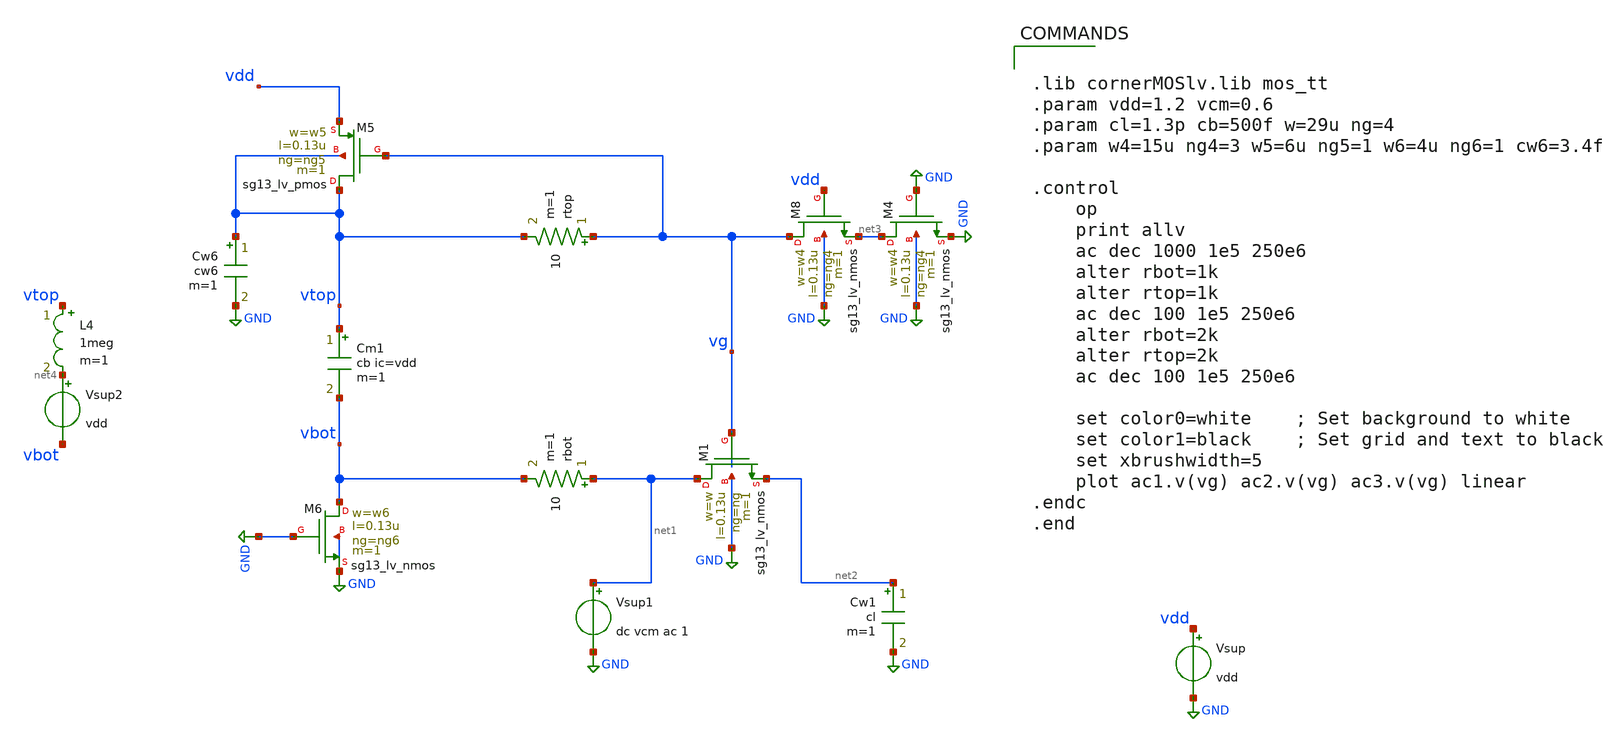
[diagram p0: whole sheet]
** sch_path: xschem/tb_boot3_ac.sch
**.subckt tb_boot3_ac
Vsup vdd GND vdd
Cm1 vtop vbot cb ic=vdd m=1
XM1 net1 vg net2 GND sg13_lv_nmos w=w l=0.13u ng=ng m=1 mm_ok=1
XM8 vg vdd net3 GND sg13_lv_nmos w=w4 l=0.13u ng=ng4 m=1 mm_ok=1
XM4 net3 GND GND GND sg13_lv_nmos w=w4 l=0.13u ng=ng4 m=1 mm_ok=1
XM6 vbot GND GND GND sg13_lv_nmos w=w6 l=0.13u ng=ng6 m=1 mm_ok=1
XM5 vtop vg vdd vtop sg13_lv_pmos w=w5 l=0.13u ng=ng5 m=1 mm_ok=1
Cw6 vtop GND cw6 m=1
Cw1 net2 GND cl m=1
Vsup1 net1 GND dc vcm ac 1
rbot net1 vbot 10 m=1
rtop vg vtop 10 m=1
Vsup2 net4 vbot vdd
L4 vtop net4 1meg m=1
**** begin user architecture code


.lib cornerMOSlv.lib mos_tt
.param vdd=1.2 vcm=0.6
.param cl=1.3p cb=500f w=29u ng=4
.param w4=15u ng4=3 w5=6u ng5=1 w6=4u ng6=1 cw6=3.4f

.control
    op
    print allv
    ac dec 1000 1e5 250e6
    alter rbot=1k
    alter rtop=1k
    ac dec 100 1e5 250e6
    alter rbot=2k
    alter rtop=2k
    ac dec 100 1e5 250e6

    set color0=white    ; Set background to white
    set color1=black    ; Set grid and text to black
    set xbrushwidth=5
    plot ac1.v(vg) ac2.v(vg) ac3.v(vg) linear
.endc
.end


**** end user architecture code
**.ends
.GLOBAL GND
.end
